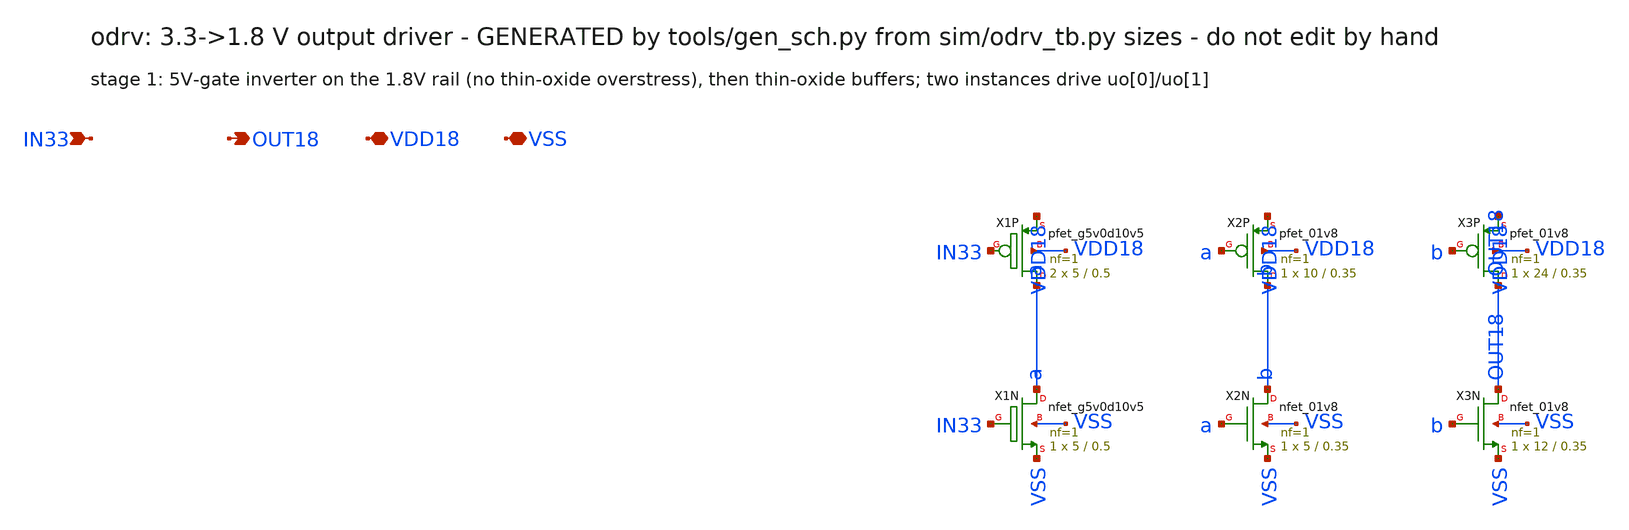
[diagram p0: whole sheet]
** sch_path: xschem/odrv.sch
**.subckt odrv IN33 OUT18 VDD18 VSS
*.ipin IN33
*.opin OUT18
*.iopin VDD18
*.iopin VSS
XX1P a IN33 VDD18 VDD18 sky130_fd_pr__pfet_g5v0d10v5 L=0.5 W=5 nf=1 ad=0 as=0 pd=0 ps=0 nrd=0 nrs=0
+ sa=0 sb=0 sd=0 mult=2 m=2
XX1N a IN33 VSS VSS sky130_fd_pr__nfet_g5v0d10v5 L=0.5 W=5 nf=1 ad=0 as=0 pd=0 ps=0 nrd=0 nrs=0 sa=0
+ sb=0 sd=0 mult=1 m=1
XX2P b a VDD18 VDD18 sky130_fd_pr__pfet_01v8 L=0.35 W=10 nf=1 ad=0 as=0 pd=0 ps=0 nrd=0 nrs=0 sa=0
+ sb=0 sd=0 mult=1 m=1
XX2N b a VSS VSS sky130_fd_pr__nfet_01v8 L=0.35 W=5 nf=1 ad=0 as=0 pd=0 ps=0 nrd=0 nrs=0 sa=0 sb=0
+ sd=0 mult=1 m=1
XX3P OUT18 b VDD18 VDD18 sky130_fd_pr__pfet_01v8 L=0.35 W=24 nf=1 ad=0 as=0 pd=0 ps=0 nrd=0 nrs=0
+ sa=0 sb=0 sd=0 mult=1 m=1
XX3N OUT18 b VSS VSS sky130_fd_pr__nfet_01v8 L=0.35 W=12 nf=1 ad=0 as=0 pd=0 ps=0 nrd=0 nrs=0 sa=0
+ sb=0 sd=0 mult=1 m=1
**.ends
.end
